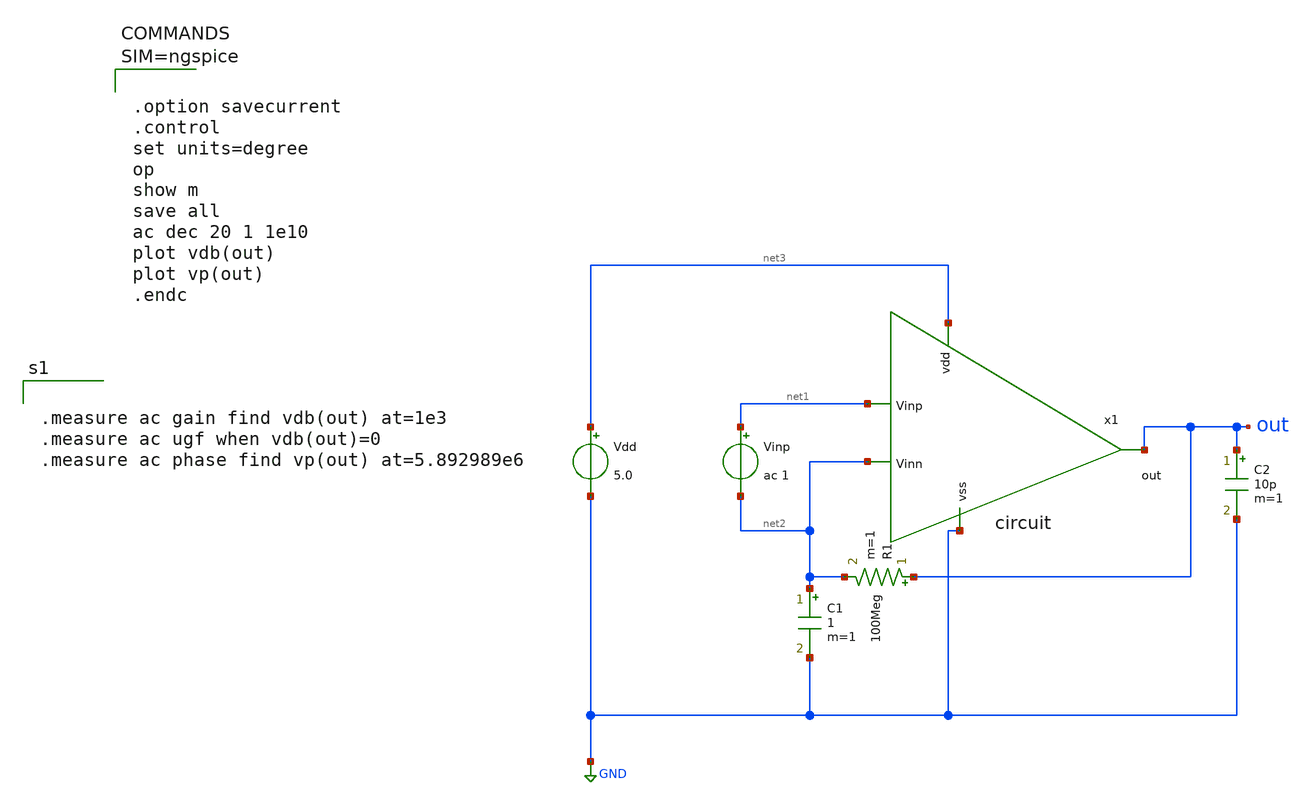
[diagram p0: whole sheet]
** sch_path: member_project/GroupWork/Team_Ando/foorests/test_circuit.sch
**.subckt test_circuit
Vinp net1 net2 ac 1
C1 net2 GND 1 m=1
R1 out net2 100Meg m=1
C2 out GND 10p m=1
Vdd net3 GND 5.0
x1 net3 out net2 net1 GND circuit
**** begin user architecture code
 .include $::LIB/mos.lib
.include $::LIB/passive.lib
.include $::LIB/diode.lib



.option savecurrent
.control
set units=degree
op
show m
save all
ac dec 20 1 1e10
plot vdb(out)
plot vp(out)
.endc





.measure ac gain find vdb(out) at=1e3
.measure ac ugf when vdb(out)=0
.measure ac phase find vp(out) at=5.892989e6

**** end user architecture code
**.ends

* expanding   symbol:  ISHI/circuit/complete/circuit.sym # of pins=5
** sym_path: member_project/GroupWork/Team_Ando/foorests/circuit.sym
** sch_path: member_project/GroupWork/Team_Ando/foorests/circuit.sch
.subckt circuit vdd out Vinn Vinp vss
*.ipin Vinn
*.ipin Vinp
*.ipin vdd
*.opin out
*.ipin vss
M1 net1 Vinn net3 net3 pmos L=2u W=200u m=1
M2 net2 Vinp net3 net3 pmos L=2u W=200u m=1
M3 net1 net1 vss vss nmos L=2u W=10u m=1
M4 net2 net1 vss vss nmos L=2u W=10u m=1
M5 net3 net4 vdd vdd pmos L=2u W=40u m=1
M6 net5 net5 vss vss nmos L=2u W=10u m=1
M7 net6 net6 net5 vss nmos L=2u W=10u m=1
M8 net6 net4 vdd vdd pmos L=2u W=20u m=1
M9 net7 net6 net2 vss nmos L=2u W=40u m=1
M10 out net4 vdd vdd pmos L=2u W=400u m=1
M11 out net2 vss vss nmos L=2u W=200u m=1
M12 net4 net4 vdd vdd pmos L=2u W=20u m=1
M13 net4 net8 vss vss nmos L=2u W=5u m=1
M14 net8 net9 vdd vdd pmos L=2u W=20u m=1
M15 net8 net8 vss vss nmos L=2u W=5u m=1
M16 net9 net9 vdd vdd pmos L=2u W=100u m=1
M17 net10 net9 vdd vdd pmos L=2u W=100u m=1
R1 vss net11 HR_poly W=4 L=20
M18 net10 net11 vss vss nmos L=2u W=20u m=1
M19 net9 net10 net11 vss nmos L=2u W=20u m=1
C2 out net7 Pdiff_cap W=18 L=10
.ends

.GLOBAL GND
.end
